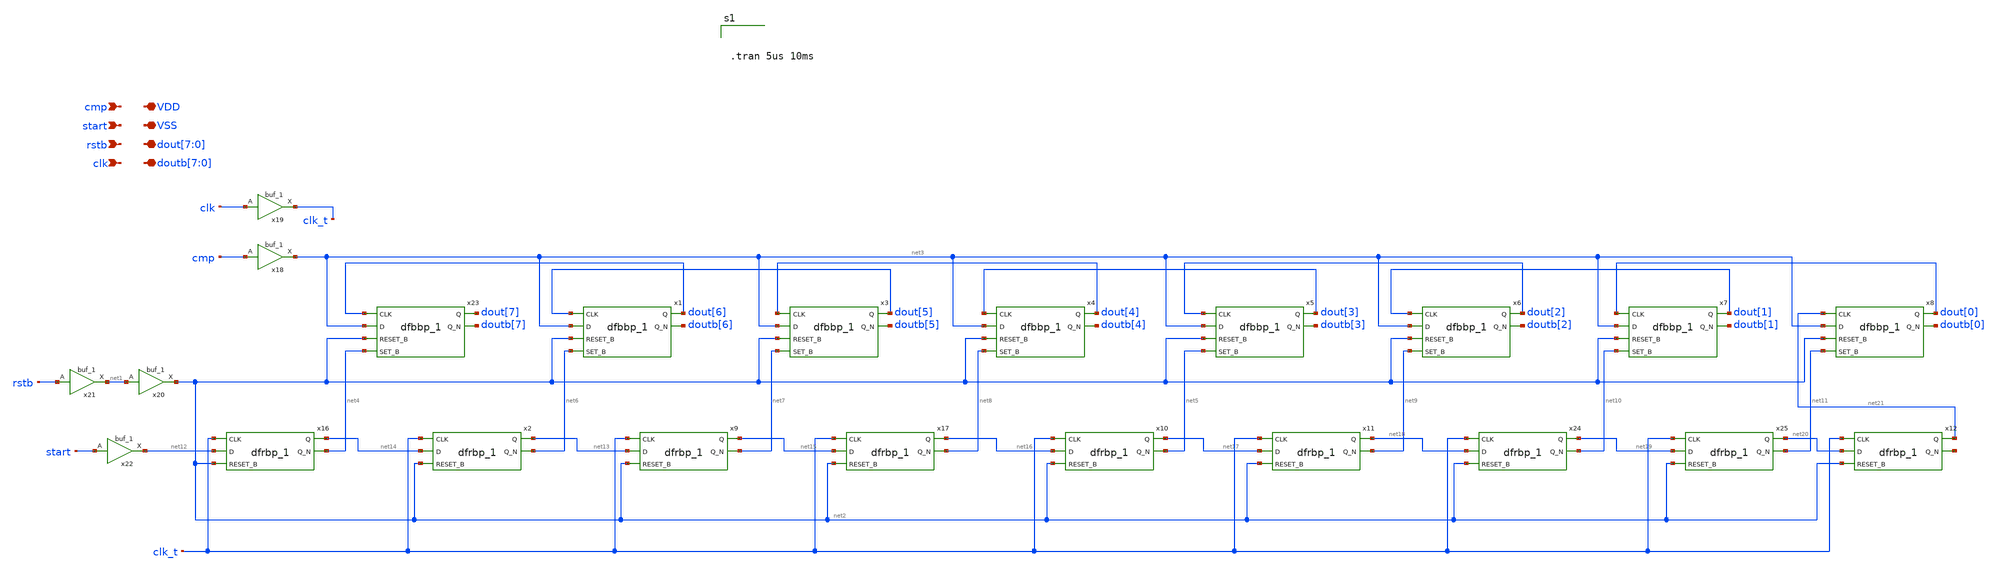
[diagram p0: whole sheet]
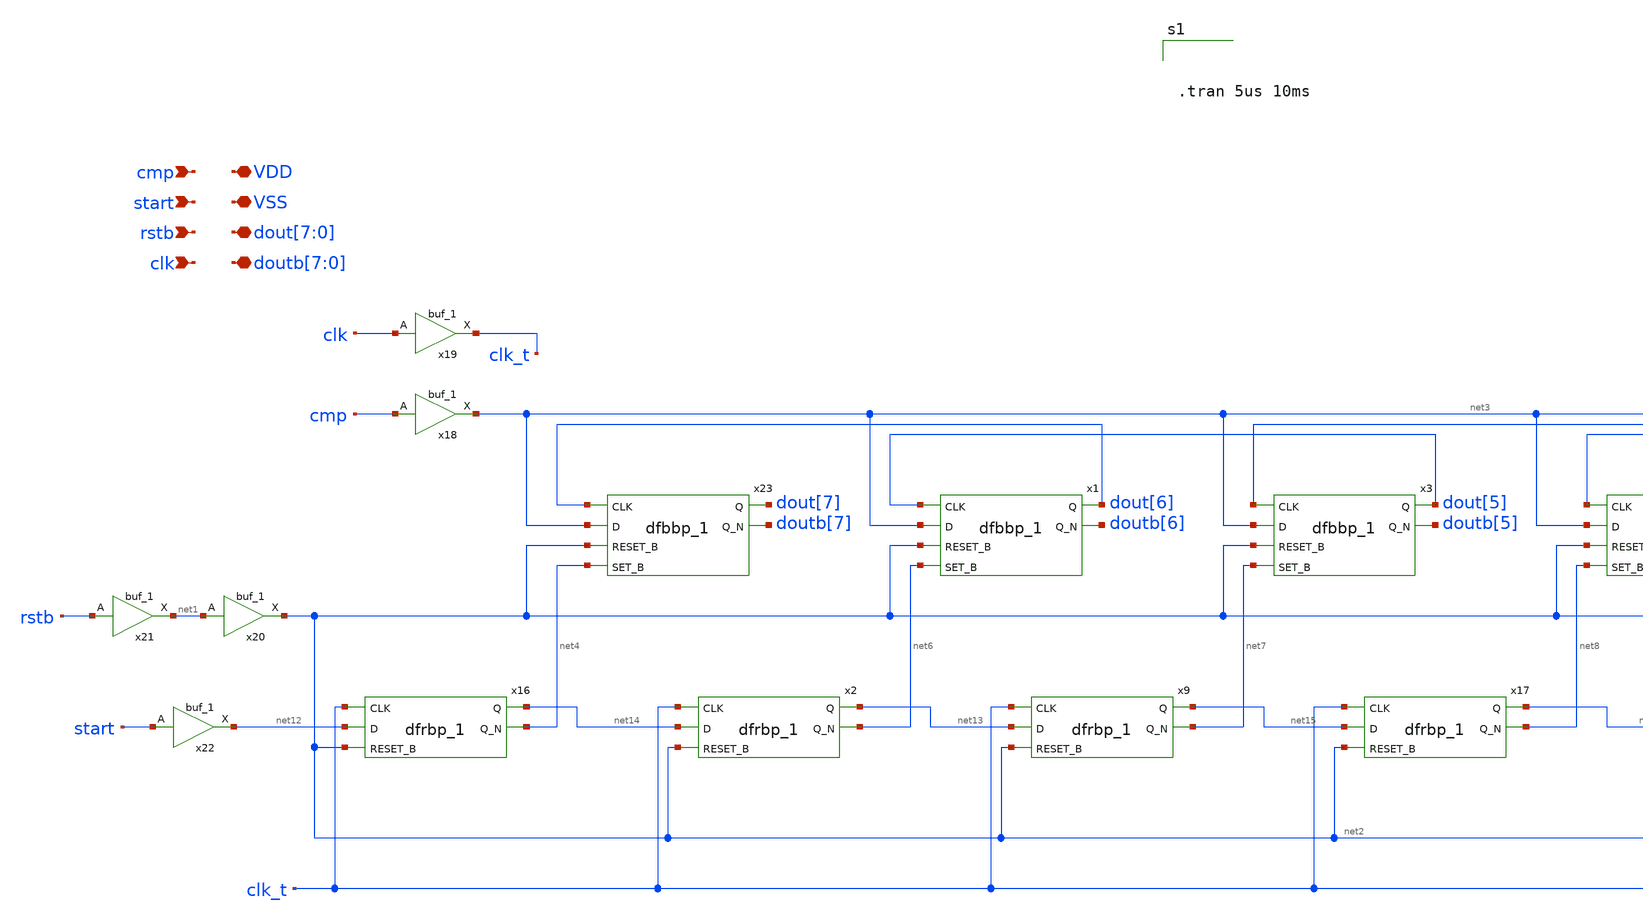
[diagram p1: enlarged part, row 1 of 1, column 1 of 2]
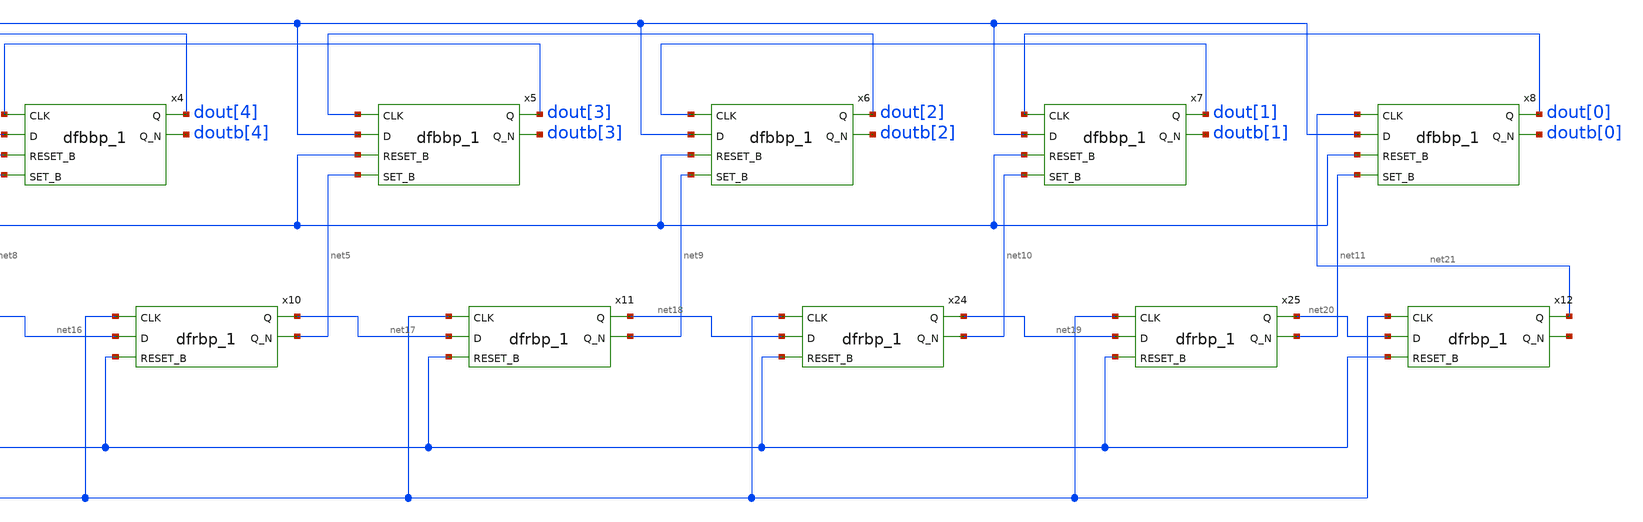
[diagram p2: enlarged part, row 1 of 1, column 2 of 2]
** sch_path: 8bitADC_SARLOGIC_dff.sch
**.subckt 8bitADC_SARLOGIC_dff cmp start rstb clk
*+ dout[7],dout[6],dout[5],dout[4],dout[3],dout[2],dout[1],dout[0] doutb[7],doutb[6],doutb[5],doutb[4],doutb[3],doutb[2],doutb[1],doutb[0] VSS VDD
*.ipin cmp
*.ipin start
*.ipin rstb
*.ipin clk
*.iopin dout[7],dout[6],dout[5],dout[4],dout[3],dout[2],dout[1],dout[0]
*.iopin doutb[7],doutb[6],doutb[5],doutb[4],doutb[3],doutb[2],doutb[1],doutb[0]
*.iopin VSS
*.iopin VDD
x18 cmp VSS VNB VPB VDD net3 sky130_fd_sc_hd__buf_1
x19 clk VSS VNB VPB VDD clk_t sky130_fd_sc_hd__buf_1
x20 net1 VSS VNB VPB VDD net2 sky130_fd_sc_hd__buf_1
x21 rstb VSS VNB VPB VDD net1 sky130_fd_sc_hd__buf_1
x22 start VSS VNB VPB VDD net12 sky130_fd_sc_hd__buf_1
x23 dout[6] net3 net2 net4 VSS VNB VPB VDD dout[7] doutb[7] sky130_fd_sc_hd__dfbbp_1
x1 dout[5] net3 net2 net6 VSS VNB VPB VDD dout[6] doutb[6] sky130_fd_sc_hd__dfbbp_1
x3 dout[4] net3 net2 net7 VSS VNB VPB VDD dout[5] doutb[5] sky130_fd_sc_hd__dfbbp_1
x4 dout[3] net3 net2 net8 VSS VNB VPB VDD dout[4] doutb[4] sky130_fd_sc_hd__dfbbp_1
x5 dout[2] net3 net2 net5 VSS VNB VPB VDD dout[3] doutb[3] sky130_fd_sc_hd__dfbbp_1
x6 dout[1] net3 net2 net9 VSS VNB VPB VDD dout[2] doutb[2] sky130_fd_sc_hd__dfbbp_1
x7 dout[0] net3 net2 net10 VSS VNB VPB VDD dout[1] doutb[1] sky130_fd_sc_hd__dfbbp_1
x8 net21 net3 net2 net11 VSS VNB VPB VDD dout[0] doutb[0] sky130_fd_sc_hd__dfbbp_1
x16 clk_t net12 net2 VSS VNB VPB VDD net14 net4 sky130_fd_sc_hd__dfrbp_1
x2 clk_t net14 net2 VSS VNB VPB VDD net13 net6 sky130_fd_sc_hd__dfrbp_1
x9 clk_t net13 net2 VSS VNB VPB VDD net15 net7 sky130_fd_sc_hd__dfrbp_1
x17 clk_t net15 net2 VSS VNB VPB VDD net16 net8 sky130_fd_sc_hd__dfrbp_1
x10 clk_t net16 net2 VSS VNB VPB VDD net17 net5 sky130_fd_sc_hd__dfrbp_1
x11 clk_t net17 net2 VSS VNB VPB VDD net18 net9 sky130_fd_sc_hd__dfrbp_1
x24 clk_t net18 net2 VSS VNB VPB VDD net19 net10 sky130_fd_sc_hd__dfrbp_1
x25 clk_t net19 net2 VSS VNB VPB VDD net20 net11 sky130_fd_sc_hd__dfrbp_1
x12 clk_t net20 net2 VSS VNB VPB VDD net21 net22 sky130_fd_sc_hd__dfrbp_1
**** begin user architecture code

** opencircuitdesign pdks install
.lib $::SKYWATER_MODELS/sky130.lib.spice tt
.include $::SKYWATER_STDCELLS/sky130_fd_sc_hd.spice





.tran 5us 10ms



**** end user architecture code
**.ends
.end
